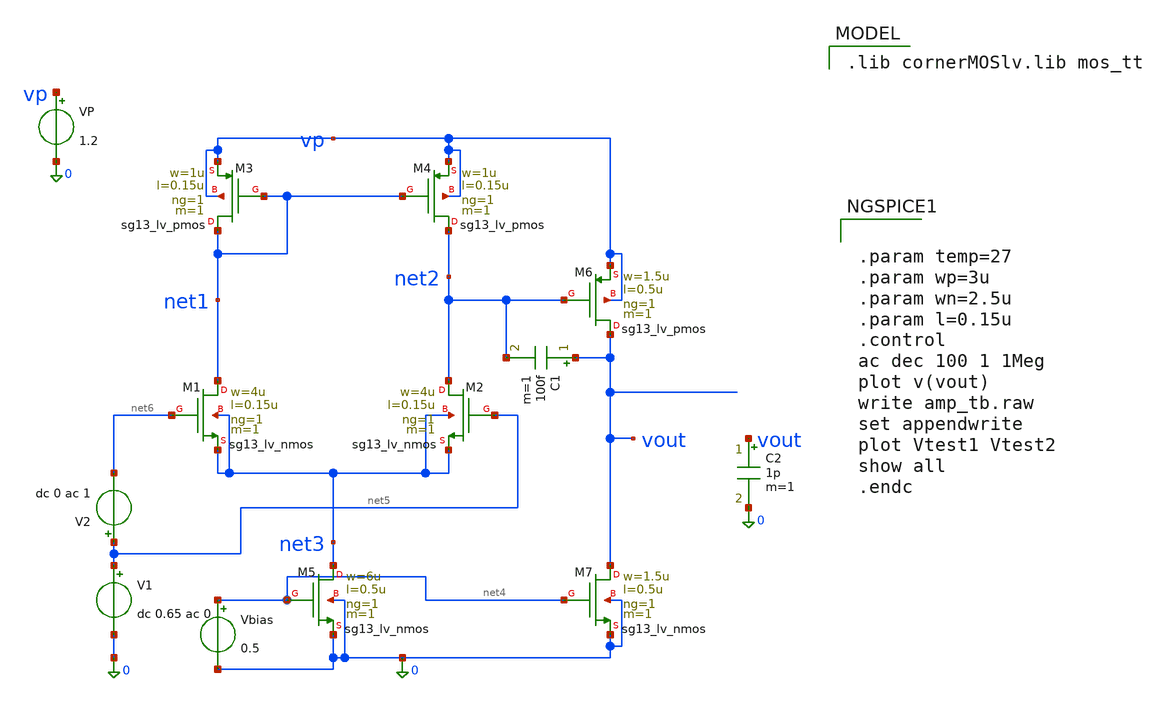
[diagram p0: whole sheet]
** sch_path: schematics/charge_pump/old_sch/amp_ac_tb.sch
**.subckt amp_ac_tb
VP vp 0 1.2
XM4 net2 net1 vp vp sg13_lv_pmos w=1u l=0.15u ng=1 m=1 mm_ok=1
XM1 net1 net6 net3 net3 sg13_lv_nmos w=4u l=0.15u ng=1 m=1 mm_ok=1
XM3 net1 net1 vp vp sg13_lv_pmos w=1u l=0.15u ng=1 m=1 mm_ok=1
XM2 net2 net5 net3 net3 sg13_lv_nmos w=4u l=0.15u ng=1 m=1 mm_ok=1
XM5 net3 net4 0 0 sg13_lv_nmos w=6u l=0.5u ng=1 m=1 mm_ok=1
XM6 vout net2 vp vp sg13_lv_pmos w=1.5u l=0.5u ng=1 m=1 mm_ok=1
XM7 vout net4 0 0 sg13_lv_nmos w=1.5u l=0.5u ng=1 m=1 mm_ok=1
Vbias net4 0 0.5
C1 vout net2 100f m=1
C2 vout 0 1p m=1
V1 net5 0 dc 0.65 ac 0
V2 net5 net6 dc 0 ac 1
**** begin user architecture code
 .lib cornerMOSlv.lib mos_tt



.param temp=27
.param wp=3u
.param wn=2.5u
.param l=0.15u
.control
ac dec 100 1 1Meg
plot v(vout)
write amp_tb.raw
set appendwrite
plot Vtest1 Vtest2
show all
.endc


**** end user architecture code
**.ends
.end
